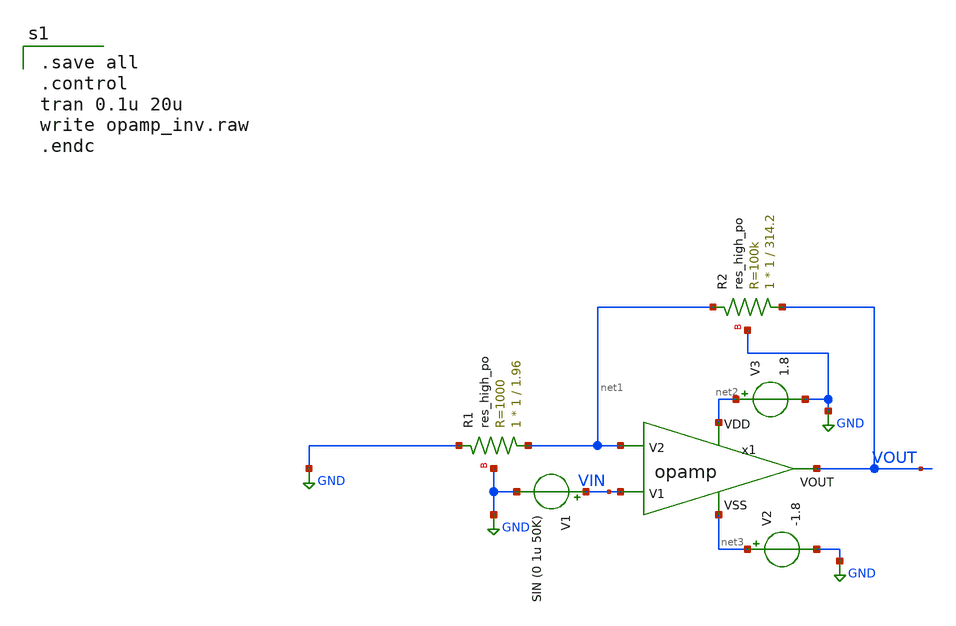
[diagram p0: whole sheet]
** sch_path: opamp_non_inv.sch
**.subckt opamp_non_inv
V2 net3 GND -1.8
V3 net2 GND 1.8
XR1 net1 GND GND sky130_fd_pr__res_high_po W=1 L=1.96 mult=1 m=1
XR2 VOUT net1 GND sky130_fd_pr__res_high_po W=1 L=314.2 mult=1 m=1
x1 net2 net1 VIN VOUT net3 opamp
V1 VIN GND SIN (0 1u 50K)
**** begin user architecture code

.save all
.control
tran 0.1u 20u
write opamp_inv.raw
.endc


** opencircuitdesign pdks install
.lib $::SKYWATER_MODELS/sky130.lib.spice tt


**** end user architecture code
**.ends

* expanding   symbol:  /foss/designs/FINAL_PROJECT_KTMDT/opamp.sym # of pins=5
** sym_path: /foss/designs/FINAL_PROJECT_KTMDT/opamp.sym
** sch_path: /foss/designs/FINAL_PROJECT_KTMDT/opamp.sch
.subckt opamp VDD V2 V1 VOUT VSS
*.ipin VSS
*.ipin VDD
*.ipin V2
*.ipin V1
*.opin VOUT
XM3 net4 V2 net1 VSS sky130_fd_pr__nfet_g5v0d10v5 L=1 W=17.45 nf=1 ad='int((nf+1)/2) * W/nf * 0.29' as='int((nf+2)/2) * W/nf * 0.29'
+ pd='2*int((nf+1)/2) * (W/nf + 0.29)' ps='2*int((nf+2)/2) * (W/nf + 0.29)' nrd='0.29 / W' nrs='0.29 / W'
+ sa=0 sb=0 sd=0 mult=1 m=1
XM1 net5 net4 VDD VDD sky130_fd_pr__pfet_g5v0d10v5 L=1 W=30 nf=1 ad='int((nf+1)/2) * W/nf * 0.29' as='int((nf+2)/2) * W/nf * 0.29'
+ pd='2*int((nf+1)/2) * (W/nf + 0.29)' ps='2*int((nf+2)/2) * (W/nf + 0.29)' nrd='0.29 / W' nrs='0.29 / W'
+ sa=0 sb=0 sd=0 mult=1 m=1
XM4 net5 V1 net1 VSS sky130_fd_pr__nfet_g5v0d10v5 L=1 W=17.45 nf=1 ad='int((nf+1)/2) * W/nf * 0.29' as='int((nf+2)/2) * W/nf * 0.29'
+ pd='2*int((nf+1)/2) * (W/nf + 0.29)' ps='2*int((nf+2)/2) * (W/nf + 0.29)' nrd='0.29 / W' nrs='0.29 / W'
+ sa=0 sb=0 sd=0 mult=1 m=1
XM6 net1 net6 VSS VSS sky130_fd_pr__nfet_g5v0d10v5 L=1 W=15.17 nf=1 ad='int((nf+1)/2) * W/nf * 0.29'
+ as='int((nf+2)/2) * W/nf * 0.29' pd='2*int((nf+1)/2) * (W/nf + 0.29)' ps='2*int((nf+2)/2) * (W/nf + 0.29)'
+ nrd='0.29 / W' nrs='0.29 / W' sa=0 sb=0 sd=0 mult=1 m=1
XM7 VOUT net6 VSS VSS sky130_fd_pr__nfet_g5v0d10v5 L=1 W=19 nf=1 ad='int((nf+1)/2) * W/nf * 0.29' as='int((nf+2)/2) * W/nf * 0.29'
+ pd='2*int((nf+1)/2) * (W/nf + 0.29)' ps='2*int((nf+2)/2) * (W/nf + 0.29)' nrd='0.29 / W' nrs='0.29 / W'
+ sa=0 sb=0 sd=0 mult=1 m=1
XM5 net6 net6 VSS VSS sky130_fd_pr__nfet_g5v0d10v5 L=1 W=15.17 nf=1 ad='int((nf+1)/2) * W/nf * 0.29'
+ as='int((nf+2)/2) * W/nf * 0.29' pd='2*int((nf+1)/2) * (W/nf + 0.29)' ps='2*int((nf+2)/2) * (W/nf + 0.29)'
+ nrd='0.29 / W' nrs='0.29 / W' sa=0 sb=0 sd=0 mult=1 m=1
XM2 net4 net4 VDD VDD sky130_fd_pr__pfet_g5v0d10v5 L=1 W=30 nf=1 ad='int((nf+1)/2) * W/nf * 0.29' as='int((nf+2)/2) * W/nf * 0.29'
+ pd='2*int((nf+1)/2) * (W/nf + 0.29)' ps='2*int((nf+2)/2) * (W/nf + 0.29)' nrd='0.29 / W' nrs='0.29 / W'
+ sa=0 sb=0 sd=0 mult=1 m=1
XM8 VOUT net5 VDD VDD sky130_fd_pr__pfet_g5v0d10v5 L=1 W=38 nf=1 ad='int((nf+1)/2) * W/nf * 0.29' as='int((nf+2)/2) * W/nf * 0.29'
+ pd='2*int((nf+1)/2) * (W/nf + 0.29)' ps='2*int((nf+2)/2) * (W/nf + 0.29)' nrd='0.29 / W' nrs='0.29 / W'
+ sa=0 sb=0 sd=0 mult=2 m=2
V_ibias net7 net6 0
.save i(v_ibias)
XR1 net2 VDD VSS sky130_fd_pr__res_high_po W=1 L=41.1 mult=1 m=1
XR2 net3 net2 VSS sky130_fd_pr__res_high_po W=1 L=41.1 mult=1 m=1
XR3 net7 net3 VSS sky130_fd_pr__res_high_po W=1 L=41.1 mult=1 m=1
XR4 net8 VOUT VSS sky130_fd_pr__res_high_po W=1 L=5 mult=1 m=1
XC1 net8 net5 sky130_fd_pr__cap_mim_m3_1 W=9 L=9 MF=2 m=2
.ends

.GLOBAL GND
.end
